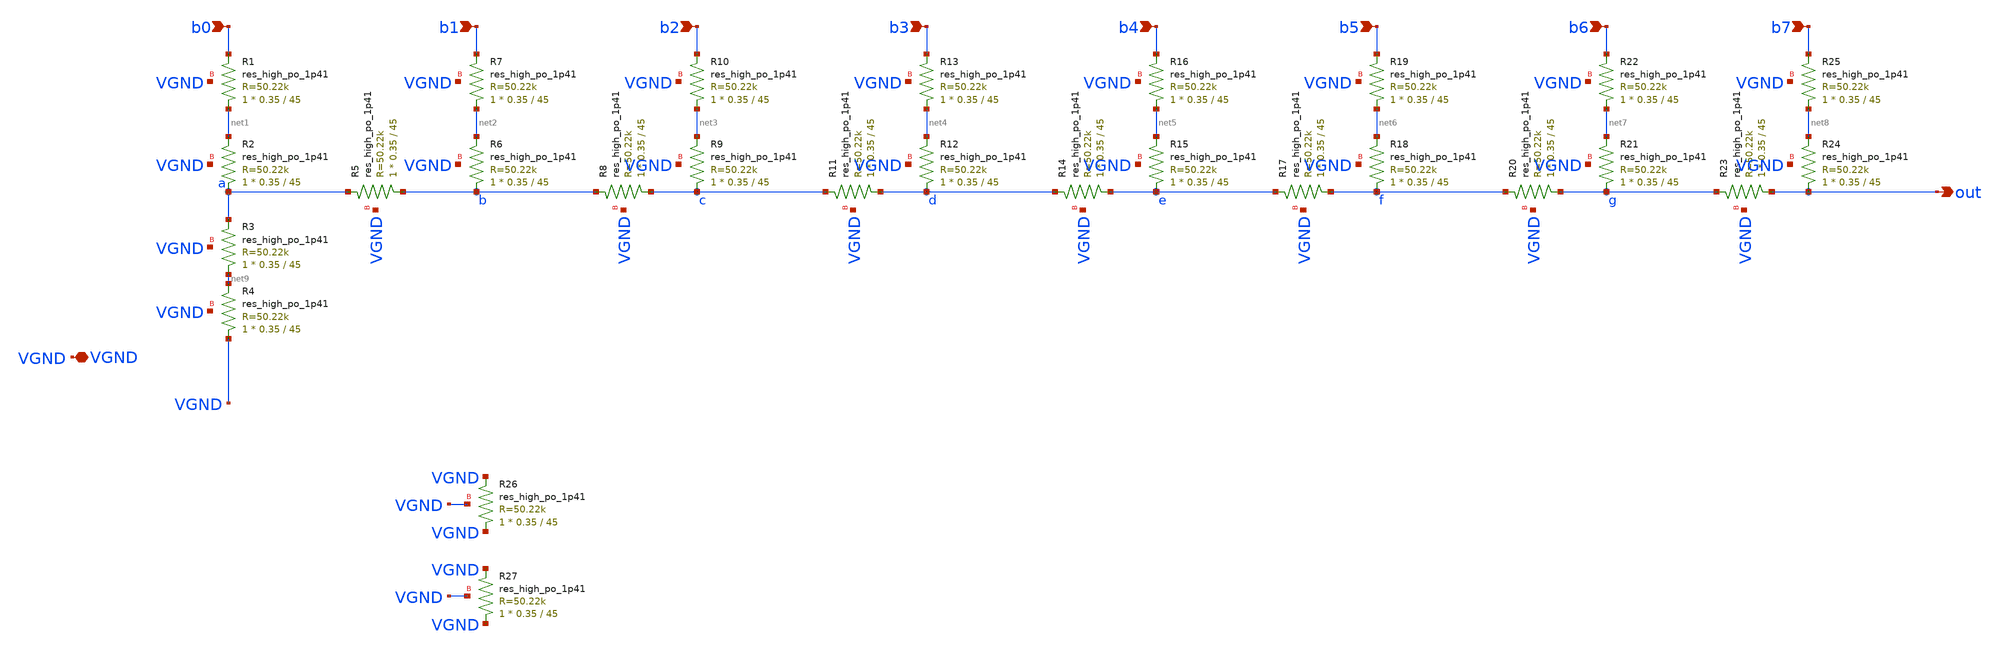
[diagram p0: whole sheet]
** sch_path: xschem/r2r.sch
**.subckt r2r b0 b1 b2 b3 b4 b5 b6 b7 out VGND
*.ipin b0
*.ipin b1
*.ipin b2
*.ipin b3
*.ipin b4
*.ipin b5
*.ipin b6
*.ipin b7
*.opin out
*.iopin VGND
XR1 net1 b0 VGND sky130_fd_pr__res_high_po_1p41 L=45 mult=1 m=1
XR7 net2 b1 VGND sky130_fd_pr__res_high_po_1p41 L=45 mult=1 m=1
XR10 net3 b2 VGND sky130_fd_pr__res_high_po_1p41 L=45 mult=1 m=1
XR13 net4 b3 VGND sky130_fd_pr__res_high_po_1p41 L=45 mult=1 m=1
XR16 net5 b4 VGND sky130_fd_pr__res_high_po_1p41 L=45 mult=1 m=1
XR19 net6 b5 VGND sky130_fd_pr__res_high_po_1p41 L=45 mult=1 m=1
XR22 net7 b6 VGND sky130_fd_pr__res_high_po_1p41 L=45 mult=1 m=1
XR25 net8 b7 VGND sky130_fd_pr__res_high_po_1p41 L=45 mult=1 m=1
XR5 b a VGND sky130_fd_pr__res_high_po_1p41 L=45 mult=1 m=1
XR8 c b VGND sky130_fd_pr__res_high_po_1p41 L=45 mult=1 m=1
XR11 d c VGND sky130_fd_pr__res_high_po_1p41 L=45 mult=1 m=1
XR14 e d VGND sky130_fd_pr__res_high_po_1p41 L=45 mult=1 m=1
XR17 f e VGND sky130_fd_pr__res_high_po_1p41 L=45 mult=1 m=1
XR20 g f VGND sky130_fd_pr__res_high_po_1p41 L=45 mult=1 m=1
XR23 out g VGND sky130_fd_pr__res_high_po_1p41 L=45 mult=1 m=1
XR3 net9 a VGND sky130_fd_pr__res_high_po_1p41 L=45 mult=1 m=1
XR2 a net1 VGND sky130_fd_pr__res_high_po_1p41 L=45 mult=1 m=1
XR6 b net2 VGND sky130_fd_pr__res_high_po_1p41 L=45 mult=1 m=1
XR9 c net3 VGND sky130_fd_pr__res_high_po_1p41 L=45 mult=1 m=1
XR12 d net4 VGND sky130_fd_pr__res_high_po_1p41 L=45 mult=1 m=1
XR15 e net5 VGND sky130_fd_pr__res_high_po_1p41 L=45 mult=1 m=1
XR18 f net6 VGND sky130_fd_pr__res_high_po_1p41 L=45 mult=1 m=1
XR21 g net7 VGND sky130_fd_pr__res_high_po_1p41 L=45 mult=1 m=1
XR24 out net8 VGND sky130_fd_pr__res_high_po_1p41 L=45 mult=1 m=1
XR4 VGND net9 VGND sky130_fd_pr__res_high_po_1p41 L=45 mult=1 m=1
XR26 VGND VGND VGND sky130_fd_pr__res_high_po_1p41 L=45 mult=1 m=1
XR27 VGND VGND VGND sky130_fd_pr__res_high_po_1p41 L=45 mult=1 m=1
**.ends
.end
